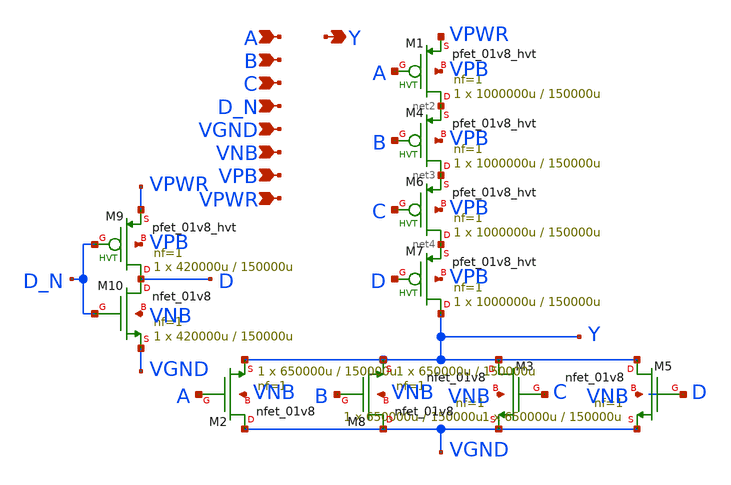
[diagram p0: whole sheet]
** sch_path: schematics/nor4b/sky130_fd_sc_hd__nor4b_1.sch
**.subckt sky130_fd_sc_hd__nor4b_1 A B C D_N VGND VNB VPB VPWR Y
*.ipin A
*.ipin B
*.ipin C
*.ipin D_N
*.ipin VGND
*.ipin VNB
*.ipin VPB
*.ipin VPWR
*.opin Y
XM1 net2 A VPWR VPB sky130_fd_pr__pfet_01v8_hvt L=150000u W=1000000u nf=1 ad='int((1 + 1)/2) * 1000000u / 1 * 0.29'
+ as='int((1 + 2)/2) * 1000000u / 1 * 0.29' pd='2*int((1 + 1)/2) * (1000000u / 1 + 0.29)' ps='2*int((1 + 2)/2) * (1000000u / 1 + 0.29)'
+ nrd='0.29 / 1000000u ' nrs='0.29 / 1000000u ' sa=0 sb=0 sd=0 mult=1 m=1
XM2 VGND A Y VNB sky130_fd_pr__nfet_01v8 L=150000u W=650000u nf=1 ad='int((1 + 1)/2) * 650000u / 1 * 0.29'
+ as='int((1 + 2)/2) * 650000u / 1 * 0.29' pd='2*int((1 + 1)/2) * (650000u / 1 + 0.29)' ps='2*int((1 + 2)/2) * (650000u / 1 + 0.29)'
+ nrd='0.29 / 650000u ' nrs='0.29 / 650000u ' sa=0 sb=0 sd=0 mult=1 m=1
XM4 net3 B net2 VPB sky130_fd_pr__pfet_01v8_hvt L=150000u W=1000000u nf=1 ad='int((1 + 1)/2) * 1000000u / 1 * 0.29'
+ as='int((1 + 2)/2) * 1000000u / 1 * 0.29' pd='2*int((1 + 1)/2) * (1000000u / 1 + 0.29)' ps='2*int((1 + 2)/2) * (1000000u / 1 + 0.29)'
+ nrd='0.29 / 1000000u ' nrs='0.29 / 1000000u ' sa=0 sb=0 sd=0 mult=1 m=1
XM3 Y C VGND VNB sky130_fd_pr__nfet_01v8 L=150000u W=650000u nf=1 ad='int((1 + 1)/2) * 650000u / 1 * 0.29'
+ as='int((1 + 2)/2) * 650000u / 1 * 0.29' pd='2*int((1 + 1)/2) * (650000u / 1 + 0.29)' ps='2*int((1 + 2)/2) * (650000u / 1 + 0.29)'
+ nrd='0.29 / 650000u ' nrs='0.29 / 650000u ' sa=0 sb=0 sd=0 mult=1 m=1
XM5 Y D VGND VNB sky130_fd_pr__nfet_01v8 L=150000u W=650000u nf=1 ad='int((1 + 1)/2) * 650000u / 1 * 0.29'
+ as='int((1 + 2)/2) * 650000u / 1 * 0.29' pd='2*int((1 + 1)/2) * (650000u / 1 + 0.29)' ps='2*int((1 + 2)/2) * (650000u / 1 + 0.29)'
+ nrd='0.29 / 650000u ' nrs='0.29 / 650000u ' sa=0 sb=0 sd=0 mult=1 m=1
XM6 net4 C net3 VPB sky130_fd_pr__pfet_01v8_hvt L=150000u W=1000000u nf=1 ad='int((1 + 1)/2) * 1000000u / 1 * 0.29'
+ as='int((1 + 2)/2) * 1000000u / 1 * 0.29' pd='2*int((1 + 1)/2) * (1000000u / 1 + 0.29)' ps='2*int((1 + 2)/2) * (1000000u / 1 + 0.29)'
+ nrd='0.29 / 1000000u ' nrs='0.29 / 1000000u ' sa=0 sb=0 sd=0 mult=1 m=1
XM7 Y D net4 VPB sky130_fd_pr__pfet_01v8_hvt L=150000u W=1000000u nf=1 ad='int((1 + 1)/2) * 1000000u / 1 * 0.29'
+ as='int((1 + 2)/2) * 1000000u / 1 * 0.29' pd='2*int((1 + 1)/2) * (1000000u / 1 + 0.29)' ps='2*int((1 + 2)/2) * (1000000u / 1 + 0.29)'
+ nrd='0.29 / 1000000u ' nrs='0.29 / 1000000u ' sa=0 sb=0 sd=0 mult=1 m=1
XM8 VGND B Y VNB sky130_fd_pr__nfet_01v8 L=150000u W=650000u nf=1 ad='int((1 + 1)/2) * 650000u / 1 * 0.29'
+ as='int((1 + 2)/2) * 650000u / 1 * 0.29' pd='2*int((1 + 1)/2) * (650000u / 1 + 0.29)' ps='2*int((1 + 2)/2) * (650000u / 1 + 0.29)'
+ nrd='0.29 / 650000u ' nrs='0.29 / 650000u ' sa=0 sb=0 sd=0 mult=1 m=1
XM9 D D_N VPWR VPB sky130_fd_pr__pfet_01v8_hvt L=150000u W=420000u nf=1 ad='int((1 + 1)/2) * 420000u / 1 * 0.29'
+ as='int((1 + 2)/2) * 420000u / 1 * 0.29' pd='2*int((1 + 1)/2) * (420000u / 1 + 0.29)' ps='2*int((1 + 2)/2) * (420000u / 1 + 0.29)'
+ nrd='0.29 / 420000u ' nrs='0.29 / 420000u ' sa=0 sb=0 sd=0 mult=1 m=1
XM10 D D_N VGND VNB sky130_fd_pr__nfet_01v8 L=150000u W=420000u nf=1 ad='int((1 + 1)/2) * 420000u / 1 * 0.29'
+ as='int((1 + 2)/2) * 420000u / 1 * 0.29' pd='2*int((1 + 1)/2) * (420000u / 1 + 0.29)' ps='2*int((1 + 2)/2) * (420000u / 1 + 0.29)'
+ nrd='0.29 / 420000u ' nrs='0.29 / 420000u ' sa=0 sb=0 sd=0 mult=1 m=1
**.ends
.end
